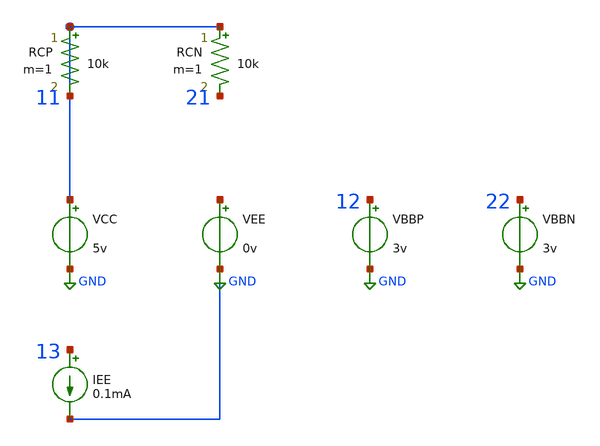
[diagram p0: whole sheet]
** sch_path: data/sch/aicas_ecp.sch
**.subckt aicas_ecp
VCC 11 GND 5v
VEE GND GND 0v
RCP 11 11 10k m=1
RCN 11 21 10k m=1
VBBP 12 GND 3v
VBBN 22 GND 3v
IEE 13 GND 0.1mA
**.ends
.GLOBAL GND
.end
